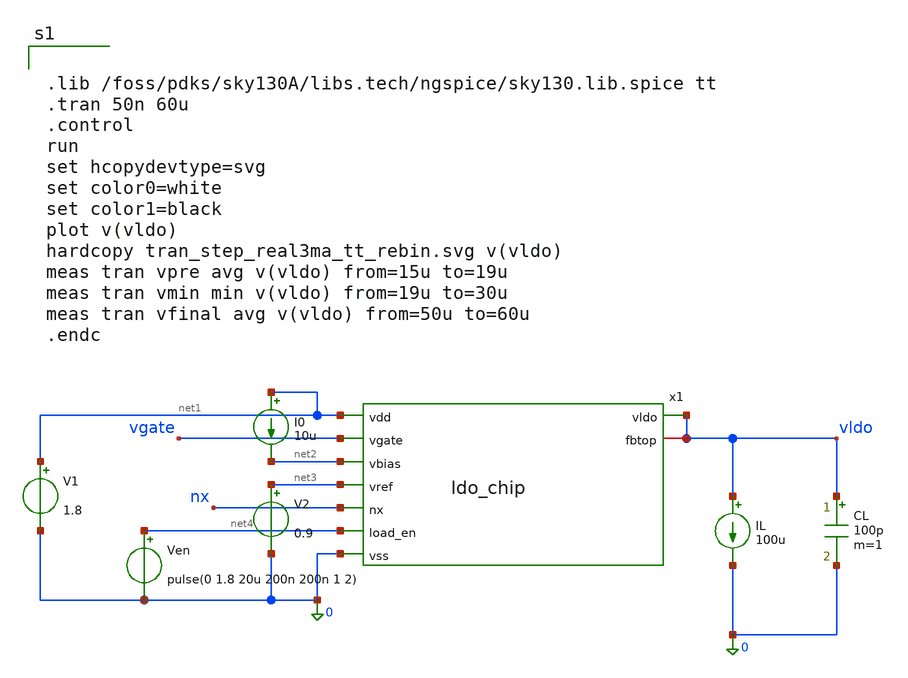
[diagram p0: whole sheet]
** sch_path: src/schematics/ldo_tran.sch
**.subckt ldo_tran
I0 net1 net2 10u
V1 net1 0 1.8
V2 net3 0 0.9
Ven net4 0 pulse(0 1.8 20u 200n 200n 1 2)
CL vldo 0 100p m=1
IL vldo 0 100u
x1 net1 vgate net2 net3 vldo vldo nx net4 0 ldo_chip
**** begin user architecture code


.lib /foss/pdks/sky130A/libs.tech/ngspice/sky130.lib.spice tt
.tran 50n 60u
.control
run
set hcopydevtype=svg
set color0=white
set color1=black
plot v(vldo)
hardcopy tran_step_real3ma_tt_rebin.svg v(vldo)
meas tran vpre avg v(vldo) from=15u to=19u
meas tran vmin min v(vldo) from=19u to=30u
meas tran vfinal avg v(vldo) from=50u to=60u
.endc


**** end user architecture code
**.ends
.end
